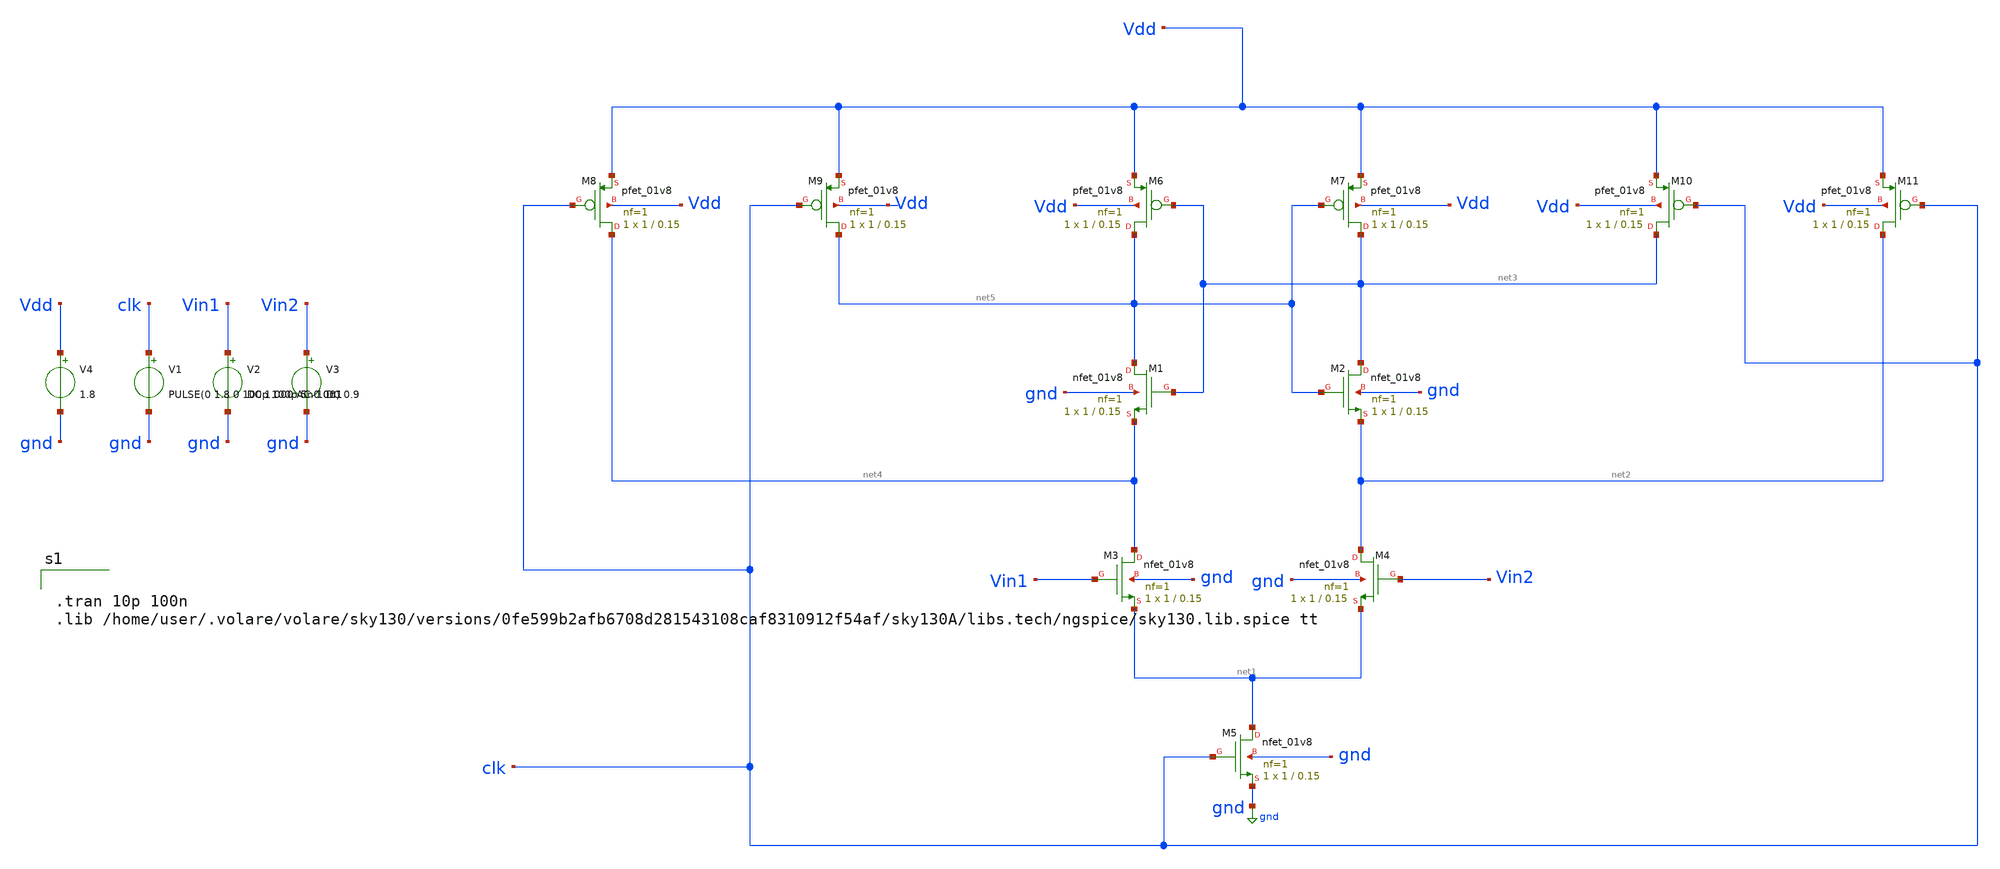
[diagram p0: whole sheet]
** sch_path: sar_adc_comparator_test/sar_adc_comparator.sch
**.subckt sar_adc_comparator
XM2 net3 net5 net2 gnd sky130_fd_pr__nfet_01v8 L=0.15 W=1 nf=1 ad='int((nf+1)/2) * W/nf * 0.29' as='int((nf+2)/2) * W/nf * 0.29'
+ pd='2*int((nf+1)/2) * (W/nf + 0.29)' ps='2*int((nf+2)/2) * (W/nf + 0.29)' nrd='0.29 / W' nrs='0.29 / W'
+ sa=0 sb=0 sd=0 mult=1 m=1
XM3 net4 Vin1 net1 gnd sky130_fd_pr__nfet_01v8 L=0.15 W=1 nf=1 ad='int((nf+1)/2) * W/nf * 0.29' as='int((nf+2)/2) * W/nf * 0.29'
+ pd='2*int((nf+1)/2) * (W/nf + 0.29)' ps='2*int((nf+2)/2) * (W/nf + 0.29)' nrd='0.29 / W' nrs='0.29 / W'
+ sa=0 sb=0 sd=0 mult=1 m=1
XM4 net2 Vin2 net1 gnd sky130_fd_pr__nfet_01v8 L=0.15 W=1 nf=1 ad='int((nf+1)/2) * W/nf * 0.29' as='int((nf+2)/2) * W/nf * 0.29'
+ pd='2*int((nf+1)/2) * (W/nf + 0.29)' ps='2*int((nf+2)/2) * (W/nf + 0.29)' nrd='0.29 / W' nrs='0.29 / W'
+ sa=0 sb=0 sd=0 mult=1 m=1
XM5 net1 clk gnd gnd sky130_fd_pr__nfet_01v8 L=0.15 W=1 nf=1 ad='int((nf+1)/2) * W/nf * 0.29' as='int((nf+2)/2) * W/nf * 0.29'
+ pd='2*int((nf+1)/2) * (W/nf + 0.29)' ps='2*int((nf+2)/2) * (W/nf + 0.29)' nrd='0.29 / W' nrs='0.29 / W'
+ sa=0 sb=0 sd=0 mult=1 m=1
XM6 net5 net3 Vdd Vdd sky130_fd_pr__pfet_01v8 L=0.15 W=1 nf=1 ad='int((nf+1)/2) * W/nf * 0.29' as='int((nf+2)/2) * W/nf * 0.29'
+ pd='2*int((nf+1)/2) * (W/nf + 0.29)' ps='2*int((nf+2)/2) * (W/nf + 0.29)' nrd='0.29 / W' nrs='0.29 / W'
+ sa=0 sb=0 sd=0 mult=1 m=1
XM7 net3 net5 Vdd Vdd sky130_fd_pr__pfet_01v8 L=0.15 W=1 nf=1 ad='int((nf+1)/2) * W/nf * 0.29' as='int((nf+2)/2) * W/nf * 0.29'
+ pd='2*int((nf+1)/2) * (W/nf + 0.29)' ps='2*int((nf+2)/2) * (W/nf + 0.29)' nrd='0.29 / W' nrs='0.29 / W'
+ sa=0 sb=0 sd=0 mult=1 m=1
XM8 net4 clk Vdd Vdd sky130_fd_pr__pfet_01v8 L=0.15 W=1 nf=1 ad='int((nf+1)/2) * W/nf * 0.29' as='int((nf+2)/2) * W/nf * 0.29'
+ pd='2*int((nf+1)/2) * (W/nf + 0.29)' ps='2*int((nf+2)/2) * (W/nf + 0.29)' nrd='0.29 / W' nrs='0.29 / W'
+ sa=0 sb=0 sd=0 mult=1 m=1
XM9 net5 clk Vdd Vdd sky130_fd_pr__pfet_01v8 L=0.15 W=1 nf=1 ad='int((nf+1)/2) * W/nf * 0.29' as='int((nf+2)/2) * W/nf * 0.29'
+ pd='2*int((nf+1)/2) * (W/nf + 0.29)' ps='2*int((nf+2)/2) * (W/nf + 0.29)' nrd='0.29 / W' nrs='0.29 / W'
+ sa=0 sb=0 sd=0 mult=1 m=1
XM10 net3 clk Vdd Vdd sky130_fd_pr__pfet_01v8 L=0.15 W=1 nf=1 ad='int((nf+1)/2) * W/nf * 0.29' as='int((nf+2)/2) * W/nf * 0.29'
+ pd='2*int((nf+1)/2) * (W/nf + 0.29)' ps='2*int((nf+2)/2) * (W/nf + 0.29)' nrd='0.29 / W' nrs='0.29 / W'
+ sa=0 sb=0 sd=0 mult=1 m=1
XM11 net2 clk Vdd Vdd sky130_fd_pr__pfet_01v8 L=0.15 W=1 nf=1 ad='int((nf+1)/2) * W/nf * 0.29' as='int((nf+2)/2) * W/nf * 0.29'
+ pd='2*int((nf+1)/2) * (W/nf + 0.29)' ps='2*int((nf+2)/2) * (W/nf + 0.29)' nrd='0.29 / W' nrs='0.29 / W'
+ sa=0 sb=0 sd=0 mult=1 m=1
XM1 net5 net3 net4 gnd sky130_fd_pr__nfet_01v8 L=0.15 W=1 nf=1 ad='int((nf+1)/2) * W/nf * 0.29' as='int((nf+2)/2) * W/nf * 0.29'
+ pd='2*int((nf+1)/2) * (W/nf + 0.29)' ps='2*int((nf+2)/2) * (W/nf + 0.29)' nrd='0.29 / W' nrs='0.29 / W'
+ sa=0 sb=0 sd=0 mult=1 m=1
V1 clk gnd PULSE(0 1.8 0 100p 100p 5n 10n)
V2 Vin1 gnd DC 1.000 AC 0.001
V3 Vin2 gnd DC 0.9
V4 Vdd gnd 1.8
**** begin user architecture code


.tran 10p 100n
.lib /home/user/.volare/volare/sky130/versions/0fe599b2afb6708d281543108caf8310912f54af/sky130A/libs.tech/ngspice/sky130.lib.spice tt

**** end user architecture code
**.ends
.GLOBAL gnd
.end
